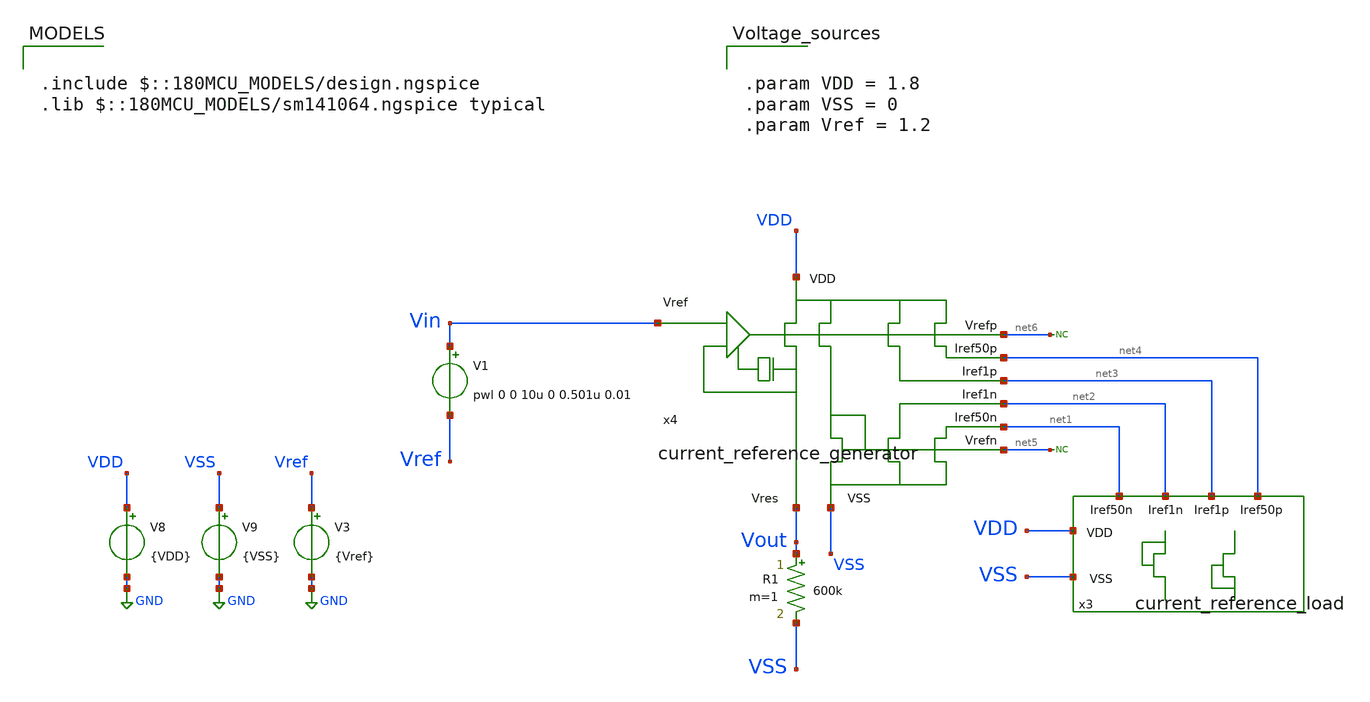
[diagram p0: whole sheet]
** sch_path: designs/current_reference_generator/xschem/current_reference_generator_TB_tran.sch
**.subckt current_reference_generator_TB_tran
V1 Vin Vref pwl 0 0 10u 0 0.501u 0.01
R1 Vout VSS 600k m=1
* noconn #net5
* noconn #net6
x3 net2 net1 net3 net4 VDD VSS current_reference_load
V8 VDD GND {VDD}
V9 VSS GND {VSS}
V3 Vref GND {Vref}
x4 VSS VDD Vin net6 net5 net2 net1 net3 net4 Vout current_reference_generator
**** begin user architecture code



.param VDD=1.8
.param Vref=1.2
.save


.control

    op

    * run tran simulation
    tran 1n 1.5u

    *let current_refp1 = v(Iref1p)/450e3

    plot v(Vout) v(Vin)

    write current_reference_generator_TB_tran.raw
.endc




.include $::180MCU_MODELS/design.ngspice
.lib $::180MCU_MODELS/sm141064.ngspice typical



.param VDD = 1.8
.param VSS = 0
.param Vref = 1.2


**** end user architecture code
**.ends
.GLOBAL GND
.end
